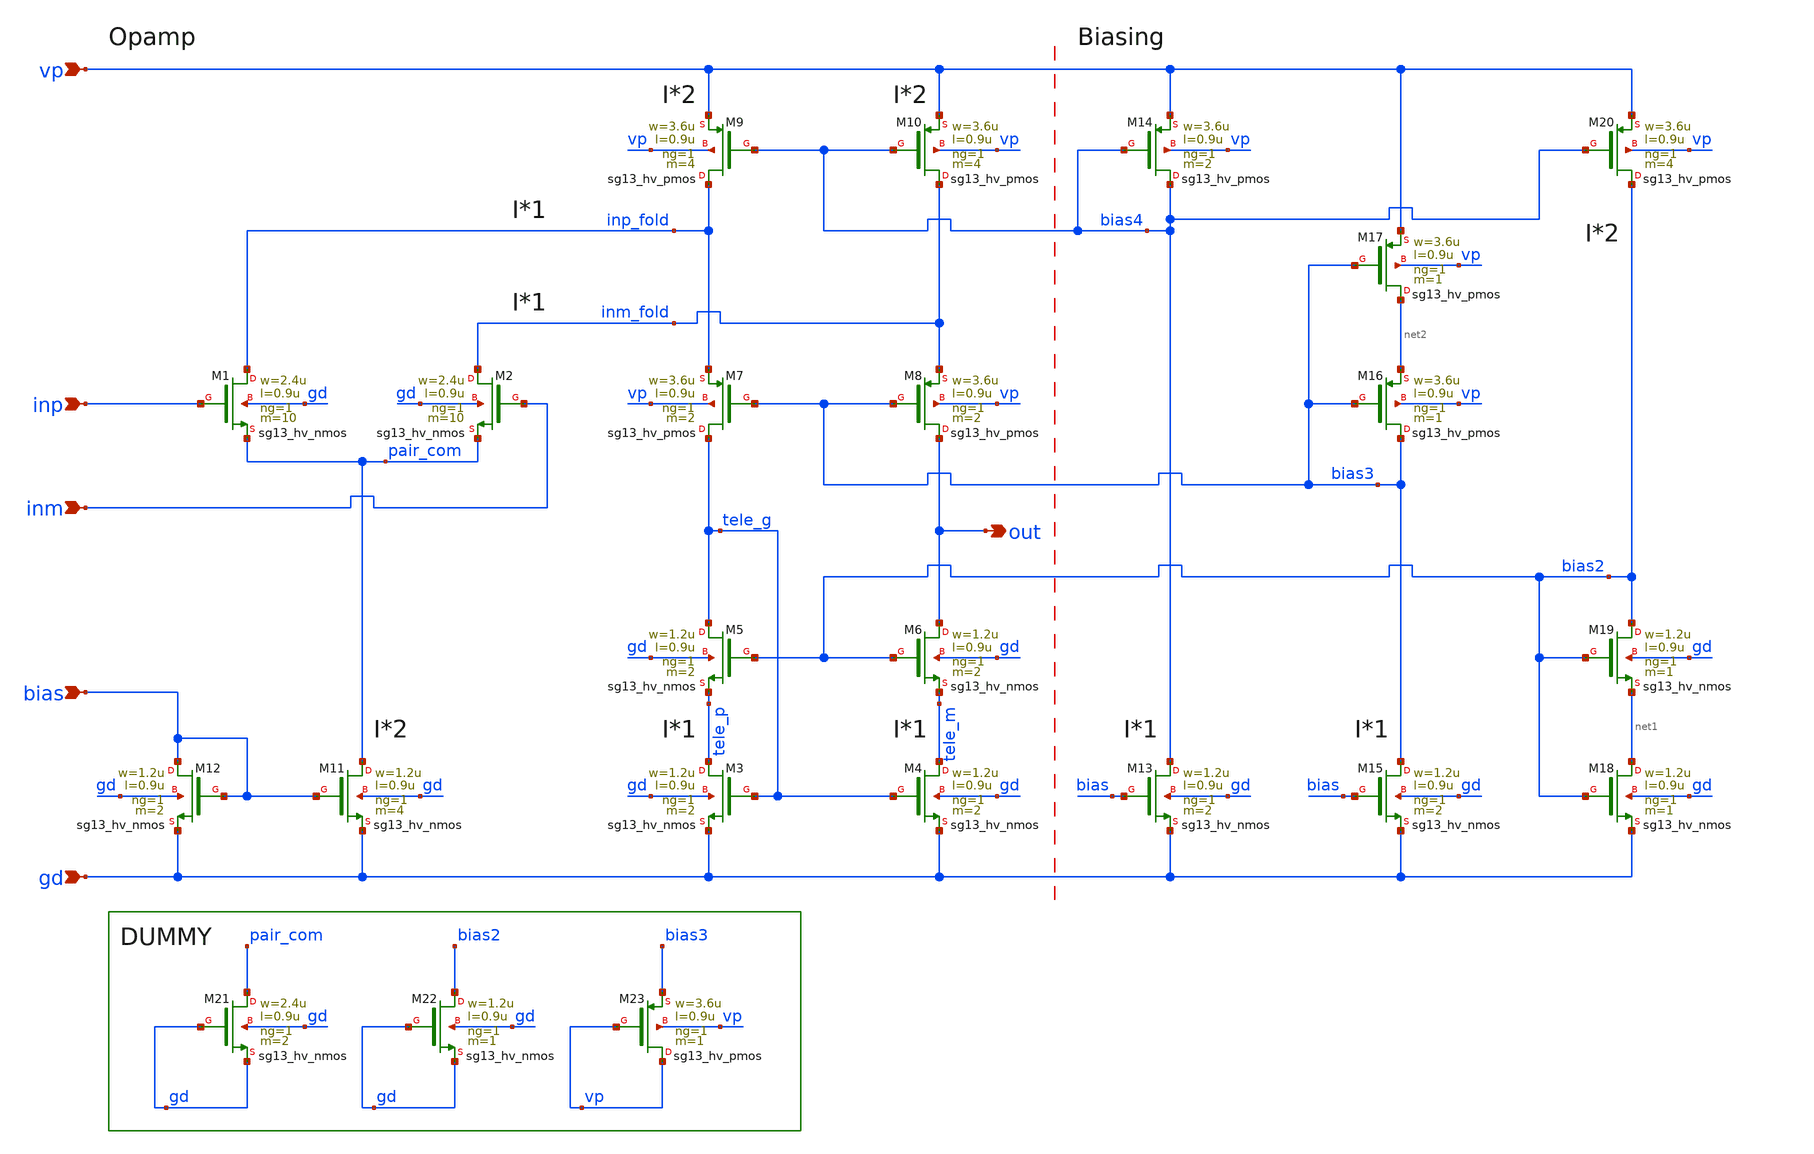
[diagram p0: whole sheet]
** sch_path: PLL0663-main/schematic/xschem/bandgap/opamp_folded_nmos.sch
**.subckt opamp_folded_nmos bias out vp inp inm gd
*.ipin bias
*.opin out
*.ipin vp
*.ipin inp
*.ipin inm
*.ipin gd
XM1 inp_fold inp pair_com gd sg13_hv_nmos w=2.4u l=0.9u ng=1 m=10 mm_ok=1
XM2 inm_fold inm pair_com gd sg13_hv_nmos w=2.4u l=0.9u ng=1 m=10 mm_ok=1
XM3 tele_p tele_g gd gd sg13_hv_nmos w=1.2u l=0.9u ng=1 m=2 mm_ok=1
XM4 tele_m tele_g gd gd sg13_hv_nmos w=1.2u l=0.9u ng=1 m=2 mm_ok=1
XM5 tele_g bias2 tele_p gd sg13_hv_nmos w=1.2u l=0.9u ng=1 m=2 mm_ok=1
XM6 out bias2 tele_m gd sg13_hv_nmos w=1.2u l=0.9u ng=1 m=2 mm_ok=1
XM7 tele_g bias3 inp_fold vp sg13_hv_pmos w=3.6u l=0.9u ng=1 m=2 mm_ok=1
XM8 out bias3 inm_fold vp sg13_hv_pmos w=3.6u l=0.9u ng=1 m=2 mm_ok=1
XM9 inp_fold bias4 vp vp sg13_hv_pmos w=3.6u l=0.9u ng=1 m=4 mm_ok=1
XM10 inm_fold bias4 vp vp sg13_hv_pmos w=3.6u l=0.9u ng=1 m=4 mm_ok=1
XM11 pair_com bias gd gd sg13_hv_nmos w=1.2u l=0.9u ng=1 m=4 mm_ok=1
XM12 bias bias gd gd sg13_hv_nmos w=1.2u l=0.9u ng=1 m=2 mm_ok=1
XM13 bias4 bias gd gd sg13_hv_nmos w=1.2u l=0.9u ng=1 m=2 mm_ok=1
XM14 bias4 bias4 vp vp sg13_hv_pmos w=3.6u l=0.9u ng=1 m=2 mm_ok=1
XM15 bias3 bias gd gd sg13_hv_nmos w=1.2u l=0.9u ng=1 m=2 mm_ok=1
XM16 bias3 bias3 net2 vp sg13_hv_pmos w=3.6u l=0.9u ng=1 m=1 mm_ok=1
XM17 net2 bias3 vp vp sg13_hv_pmos w=3.6u l=0.9u ng=1 m=1 mm_ok=1
XM18 net1 bias2 gd gd sg13_hv_nmos w=1.2u l=0.9u ng=1 m=1 mm_ok=1
XM19 bias2 bias2 net1 gd sg13_hv_nmos w=1.2u l=0.9u ng=1 m=1 mm_ok=1
XM20 bias2 bias4 vp vp sg13_hv_pmos w=3.6u l=0.9u ng=1 m=4 mm_ok=1
XM21 pair_com gd gd gd sg13_hv_nmos w=2.4u l=0.9u ng=1 m=2 mm_ok=1
XM22 bias2 gd gd gd sg13_hv_nmos w=1.2u l=0.9u ng=1 m=1 mm_ok=1
XM23 vp vp bias3 vp sg13_hv_pmos w=3.6u l=0.9u ng=1 m=1 mm_ok=1
**.ends
.end
